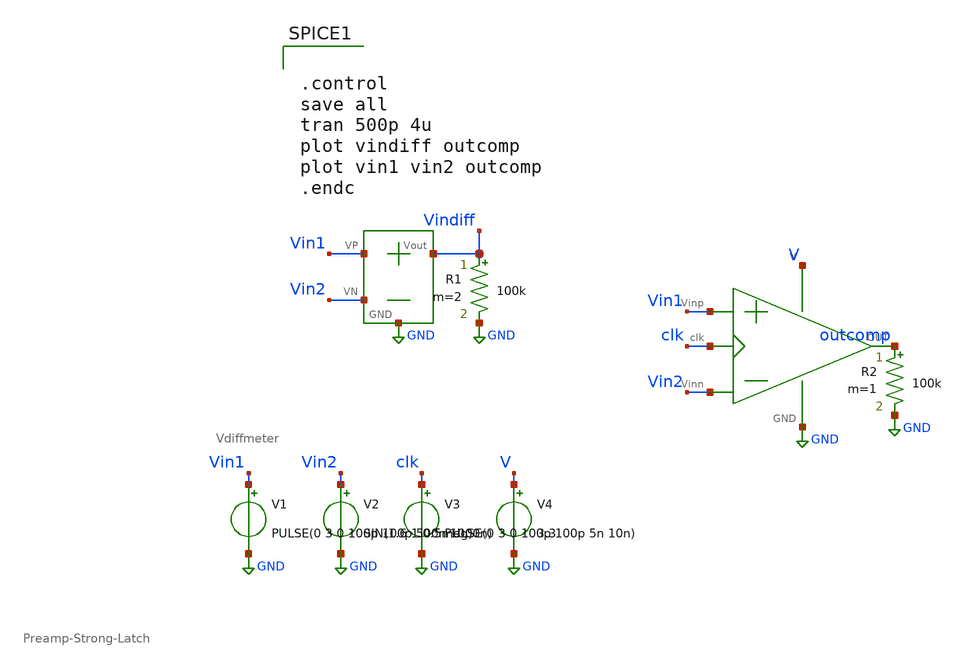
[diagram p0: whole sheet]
** sch_path: SAR_ADC/xschem/test/comp_full_tb/pulse_1meg-sin0meg5__tb.sch
**.subckt pulse_1meg-sin0meg5__tb
X1 V GND Vin1 Vin2 outcomp clk Preamp-Strong-Latch
V1 Vin1 GND PULSE(0 3 0 100p 100p 500n 1000n)
V2 Vin2 GND SIN(1.6 1 0.5meg)
V3 clk GND PULSE(0 3 0 100p 100p 5n 10n)
V4 V GND 3.3
X2 Vin1 Vin2 Vindiff GND Vdiffmeter
R1 Vindiff GND 100k m=2
R2 outcomp GND 100k m=1
**** begin user architecture code


.control
save all
tran 500p 4u
plot vindiff outcomp
plot vin1 vin2 outcomp
.endc


.include /foss/pdks/gf180mcuC/libs.tech/ngspice/design.ngspice
.lib /foss/pdks/gf180mcuC/libs.tech/ngspice/sm141064.ngspice typical

**** end user architecture code
**.ends
.GLOBAL GND
.end
